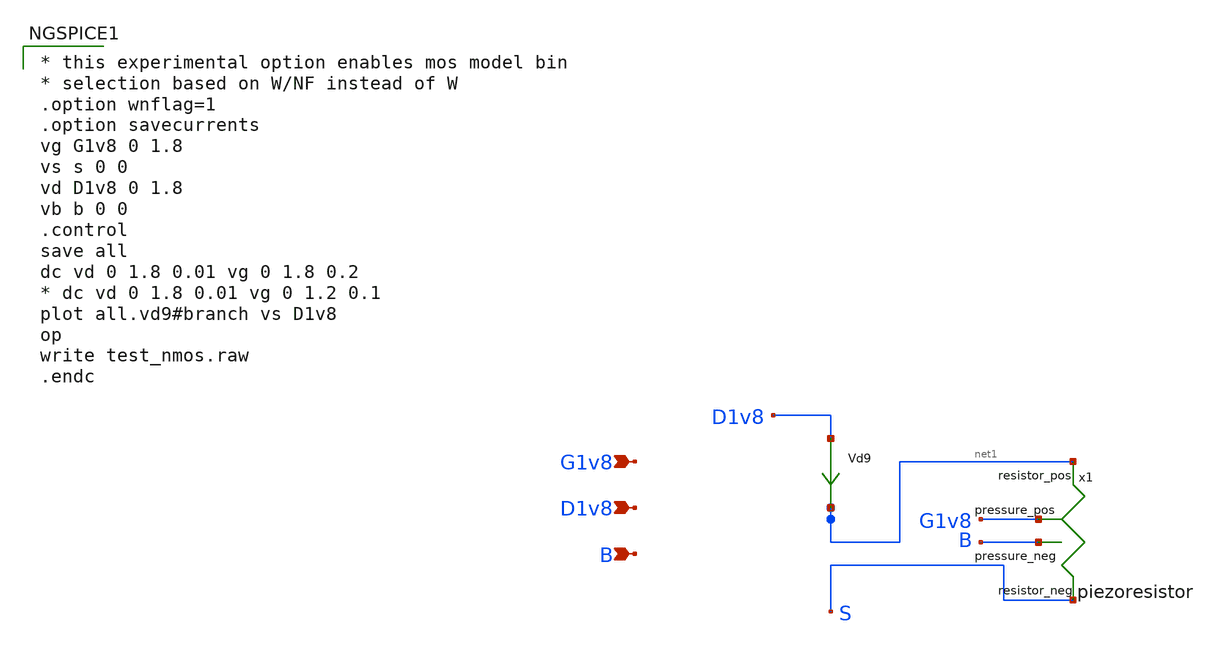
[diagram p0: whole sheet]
** sch_path: piezoresistor_tb.sch
* Copyright 2020 Stefan Frederik Schippers
* Licensed under the Apache License, Version 2.0 (the "License");
* you may not use this file except in compliance with the License.
* You may obtain a copy of the License at
* https://www.apache.org/licenses/LICENSE-2.0
* Unless required by applicable law or agreed to in writing, software
* distributed under the License is distributed on an "AS IS" BASIS,
* WITHOUT WARRANTIES OR CONDITIONS OF ANY KIND, either express or implied.
* See the License for the specific language governing permissions and
* limitations under the License.
**.subckt piezoresistor_tb G1v8 D1v8 B
*.ipin G1v8
*.ipin D1v8
*.ipin B
Vd9 D1v8 net1 0
.save i(vd9)
x1 G1v8 B net1 S piezoresistor
**** begin user architecture code

* this experimental option enables mos model bin
* selection based on W/NF instead of W
.option wnflag=1
.option savecurrents
vg G1v8 0 1.8
vs s 0 0
vd D1v8 0 1.8
vb b 0 0
.control
save all
dc vd 0 1.8 0.01 vg 0 1.8 0.2
* dc vd 0 1.8 0.01 vg 0 1.2 0.1
plot all.vd9#branch vs D1v8
op
write test_nmos.raw
.endc


**** end user architecture code
**.ends

* expanding   symbol:  /home/mast/Progetti/Telluride2021/sky130_TAC3/piezoresistor.sym # of pins=4
** sym_path: piezoresistor.sym
** sch_path: piezoresistor.sch
.subckt piezoresistor pressure_pos pressure_neg resistor_pos resistor_neg
*.ipin pressure_pos
*.ipin pressure_neg
*.iopin resistor_pos
*.iopin resistor_neg
Broot sqrtp 0 V = sqrt(v(pressure_pos,pressure_neg))
Bres res 0 V = 106*(50/v(sqrtp)-1)*exp(-0.328*v(sqrtp))+15
Brvar resistor_pos resistor_neg I = V(resistor_pos,resistor_neg)/V(res)
.ends

.end
